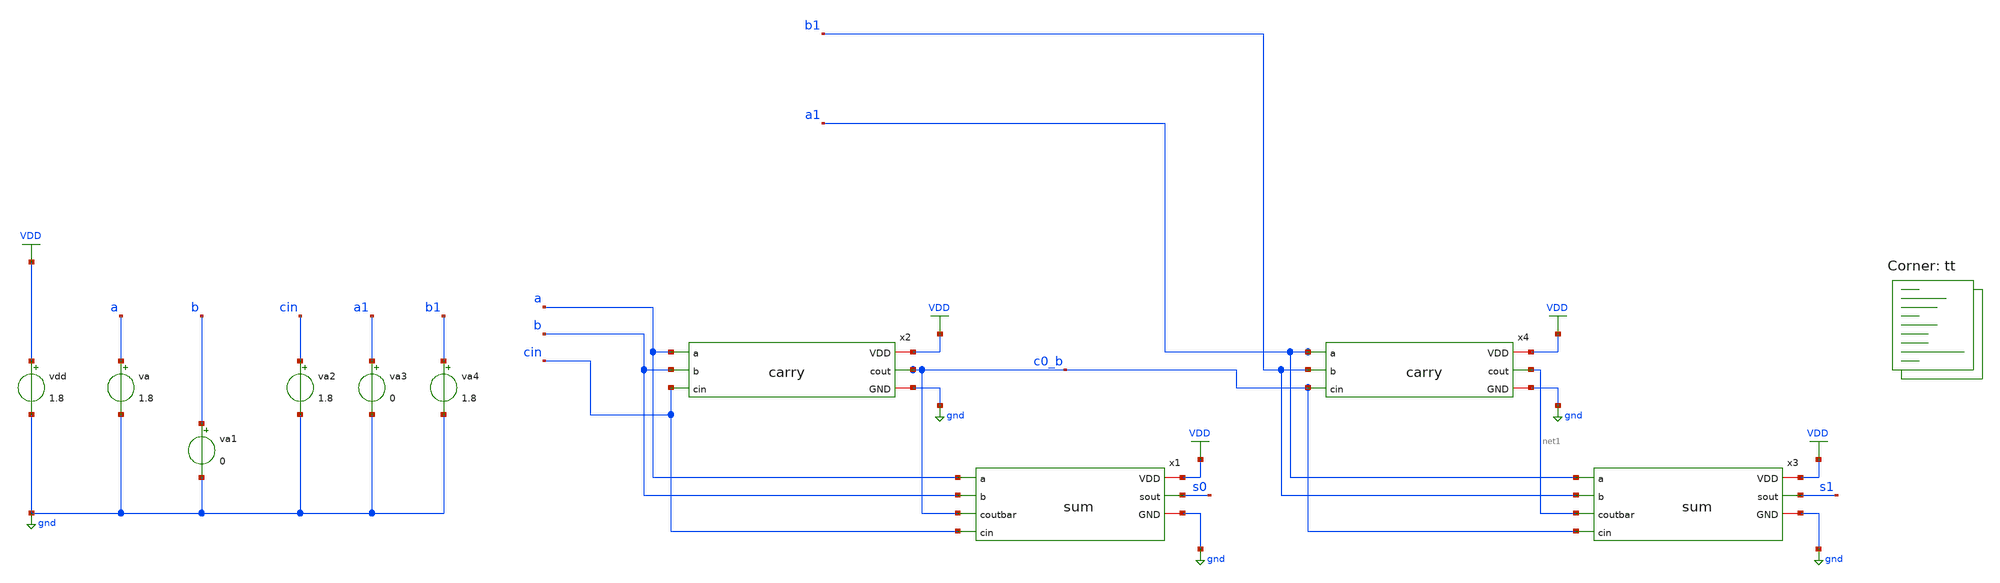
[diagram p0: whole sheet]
** sch_path: assignments/assignment8/assign1a.sch
**.subckt assign1a
x1 VDD a b c0_b cin s0 gnd sum
x2 VDD a b cin c0_b gnd carry
x3 VDD a1 b1 net1 c0_b s1 gnd sum
x4 VDD a1 b1 c0_b net1 gnd carry
vdd VDD gnd 1.8
va a gnd 1.8
va1 b gnd 0
va2 cin gnd 1.8
va3 a1 gnd 0
va4 b1 gnd 1.8
**** begin user architecture code


.include carry_extracted.spice
.include sum_extracted.spice
.control
* alter @va[pulse] = [ 1.8 0 0 0 0 4n 8n]
* alter @va1[pulse] = [ 1.8 0 0 0 0 4n 8n]
alter @va2[pulse] = [ 0 1.8 0 10p 10p 4n 8n ]
* alter @va3[pulse] = [ 1.8 0 0 0 0 4n 8n]
* alter @va4[pulse] = [ 1.8 0 0 0 0 4n 8n]

tran 1p 20n
meas tran delay_cin_net1 TRIG v(cin) VAL=0.9 RISE=3 TARG v(c0_b) VAL=0.9 FALL=3
meas tran delay_cin_s0 TRIG v(cin) VAL=0.9 RISE=3 TARG v(s0) VAL=0.9 RISE=3
plot v(cin) v(s0)
print delay_cin_net1 delay_cin_s0
.endc


.lib $::SKYWATER_MODELS/sky130.lib.spice tt
**** end user architecture code
**.ends
.GLOBAL VDD
.GLOBAL gnd
.end
